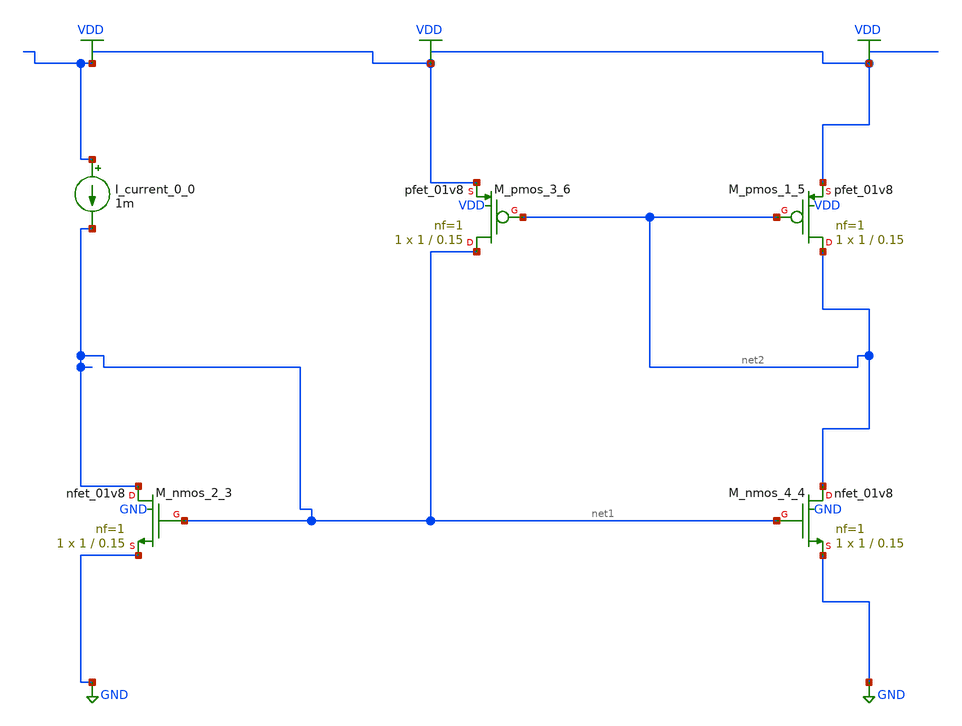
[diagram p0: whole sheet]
** sch_path: schematics/AMSNet/335.sch
**.subckt 335
I_current_0_0 VDD net1 1m
XM_nmos_2_3 net1 net1 GND GND sky130_fd_pr__nfet_01v8 L=0.15 W=1 nf=1 ad='int((1 + 1)/2) * 1 / 1 * 0.29'
+ as='int((1 + 2)/2) * 1 / 1 * 0.29' pd='2*int((1 + 1)/2) * (1 / 1 + 0.29)' ps='2*int((1 + 2)/2) * (1 / 1 + 0.29)'
+ nrd='0.29 / 1 ' nrs='0.29 / 1 ' sa=0 sb=0 sd=0 mult=1 m=1
XM_nmos_4_4 net2 net1 GND GND sky130_fd_pr__nfet_01v8 L=0.15 W=1 nf=1 ad='int((1 + 1)/2) * 1 / 1 * 0.29'
+ as='int((1 + 2)/2) * 1 / 1 * 0.29' pd='2*int((1 + 1)/2) * (1 / 1 + 0.29)' ps='2*int((1 + 2)/2) * (1 / 1 + 0.29)'
+ nrd='0.29 / 1 ' nrs='0.29 / 1 ' sa=0 sb=0 sd=0 mult=1 m=1
XM_pmos_1_5 net2 net2 VDD VDD sky130_fd_pr__pfet_01v8 L=0.15 W=1 nf=1 ad='int((1 + 1)/2) * 1 / 1 * 0.29'
+ as='int((1 + 2)/2) * 1 / 1 * 0.29' pd='2*int((1 + 1)/2) * (1 / 1 + 0.29)' ps='2*int((1 + 2)/2) * (1 / 1 + 0.29)'
+ nrd='0.29 / 1 ' nrs='0.29 / 1 ' sa=0 sb=0 sd=0 mult=1 m=1
XM_pmos_3_6 net1 net2 VDD VDD sky130_fd_pr__pfet_01v8 L=0.15 W=1 nf=1 ad='int((1 + 1)/2) * 1 / 1 * 0.29'
+ as='int((1 + 2)/2) * 1 / 1 * 0.29' pd='2*int((1 + 1)/2) * (1 / 1 + 0.29)' ps='2*int((1 + 2)/2) * (1 / 1 + 0.29)'
+ nrd='0.29 / 1 ' nrs='0.29 / 1 ' sa=0 sb=0 sd=0 mult=1 m=1
**.ends
.GLOBAL GND
.GLOBAL VDD
.end
